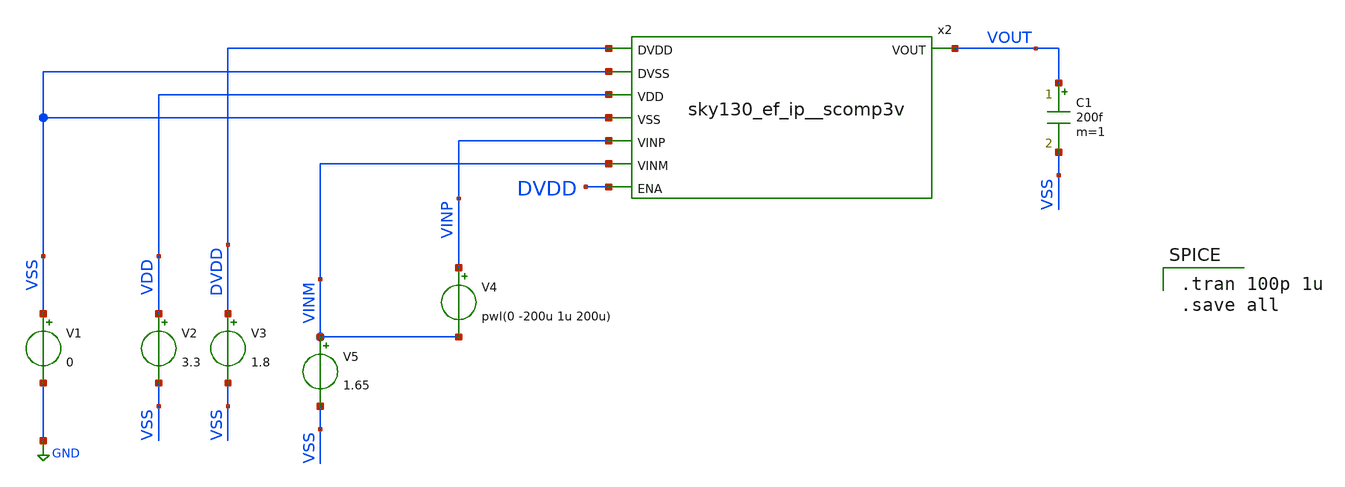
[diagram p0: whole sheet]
** sch_path: xschem/sky130_ef_ip__scomp3v_tb.sch
**.subckt sky130_ef_ip__scomp3v_tb
V1 VSS GND 0
V2 VDD VSS 3.3
C1 VOUT VSS 200f m=1
V4 VINP VINM pwl(0 -200u 1u 200u)
V5 VINM VSS 1.65
x2 VOUT DVDD VSS VDD VSS VINP VINM DVDD sky130_ef_ip__scomp3v
V3 DVDD VSS 1.8
**** begin user architecture code
.lib $::SKYWATER_MODELS/sky130.lib.spice tt

.tran 100p 1u
.save all



.include /usr/share/pdk/sky130A/libs.ref/sky130_fd_sc_hvl/spice/sky130_fd_sc_hvl.spice

**** end user architecture code
**.ends
.GLOBAL GND
.end
